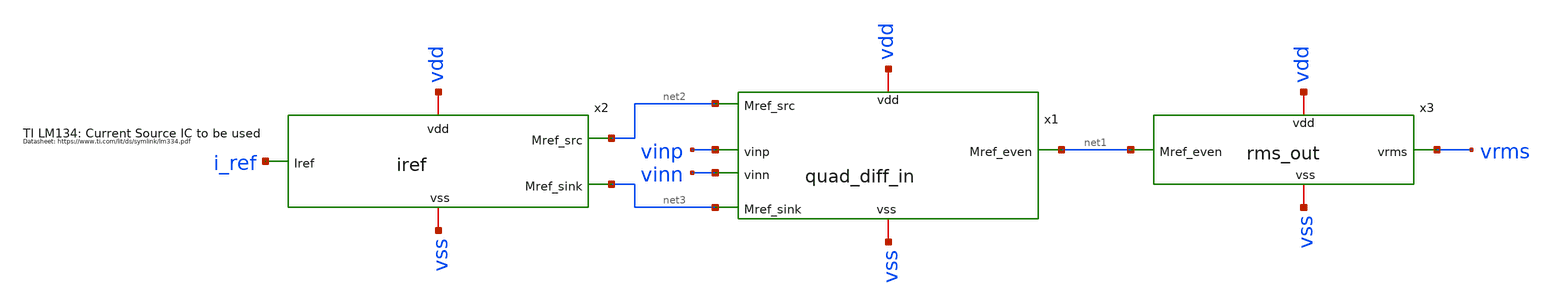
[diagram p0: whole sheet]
** sch_path: designs/libs/tb_analog/tb_rms_det/tb_rms_det.sch
**.subckt tb_rms_det
x1 vdd net2 net1 vinp vinn net3 vss quad_diff_in
x2 vdd net2 i_ref net3 vss iref
x3 vdd net1 vrms vss rms_out
**.ends

* expanding   symbol:  libs/core_analog/quad_diff_in/quad_diff_in.sym # of pins=7
** sym_path: designs/libs/core_analog/quad_diff_in/quad_diff_in.sym
** sch_path: designs/libs/core_analog/quad_diff_in/quad_diff_in.sch
.subckt quad_diff_in vdd Mref_src Mref_even vinp vinn Mref_sink vss
*.iopin vdd
*.iopin vss
*.ipin vinp
*.ipin vinn
*.ipin Mref_src
*.ipin Mref_sink
*.opin Mref_even
XM1 net3 vinp net2 vss nfet_03v3 L=0.28u W=0.22u nf=1 ad='int((nf+1)/2) * W/nf * 0.18u' as='int((nf+2)/2) * W/nf * 0.18u'
+ pd='2*int((nf+1)/2) * (W/nf + 0.18u)' ps='2*int((nf+2)/2) * (W/nf + 0.18u)' nrd='0.18u / W' nrs='0.18u / W'
+ sa=0 sb=0 sd=0 m=1
XM2 Mref_even Mref_even vdd vdd pfet_03v3 L=0.28u W=0.22u nf=1 ad='int((nf+1)/2) * W/nf * 0.18u' as='int((nf+2)/2) * W/nf * 0.18u'
+ pd='2*int((nf+1)/2) * (W/nf + 0.18u)' ps='2*int((nf+2)/2) * (W/nf + 0.18u)' nrd='0.18u / W' nrs='0.18u / W'
+ sa=0 sb=0 sd=0 m=1
XM3 net3 vinn net1 vss nfet_03v3 L=0.28u W=0.22u nf=1 ad='int((nf+1)/2) * W/nf * 0.18u' as='int((nf+2)/2) * W/nf * 0.18u'
+ pd='2*int((nf+1)/2) * (W/nf + 0.18u)' ps='2*int((nf+2)/2) * (W/nf + 0.18u)' nrd='0.18u / W' nrs='0.18u / W'
+ sa=0 sb=0 sd=0 m=1
XM4 vdd vinp net1 vss nfet_03v3 L=0.28u W=0.22u nf=1 ad='int((nf+1)/2) * W/nf * 0.18u' as='int((nf+2)/2) * W/nf * 0.18u'
+ pd='2*int((nf+1)/2) * (W/nf + 0.18u)' ps='2*int((nf+2)/2) * (W/nf + 0.18u)' nrd='0.18u / W' nrs='0.18u / W'
+ sa=0 sb=0 sd=0 m=1
XM5 vdd vinn net2 vss nfet_03v3 L=0.28u W=0.22u nf=1 ad='int((nf+1)/2) * W/nf * 0.18u' as='int((nf+2)/2) * W/nf * 0.18u'
+ pd='2*int((nf+1)/2) * (W/nf + 0.18u)' ps='2*int((nf+2)/2) * (W/nf + 0.18u)' nrd='0.18u / W' nrs='0.18u / W'
+ sa=0 sb=0 sd=0 m=1
even_curr Mref_even net3 0
.save i(even_curr)
XM6 net4 Mref_src vdd vdd pfet_03v3 L=0.28u W=0.22u nf=1 ad='int((nf+1)/2) * W/nf * 0.18u' as='int((nf+2)/2) * W/nf * 0.18u'
+ pd='2*int((nf+1)/2) * (W/nf + 0.18u)' ps='2*int((nf+2)/2) * (W/nf + 0.18u)' nrd='0.18u / W' nrs='0.18u / W'
+ sa=0 sb=0 sd=0 m=1
dc_bias net4 Mref_even 0
.save i(dc_bias)
XM7 net1 Mref_sink vss vss nfet_03v3 L=0.28u W=0.22u nf=1 ad='int((nf+1)/2) * W/nf * 0.18u' as='int((nf+2)/2) * W/nf * 0.18u'
+ pd='2*int((nf+1)/2) * (W/nf + 0.18u)' ps='2*int((nf+2)/2) * (W/nf + 0.18u)' nrd='0.18u / W' nrs='0.18u / W'
+ sa=0 sb=0 sd=0 m=1
XM8 net2 Mref_sink vss vss nfet_03v3 L=0.28u W=0.22u nf=1 ad='int((nf+1)/2) * W/nf * 0.18u' as='int((nf+2)/2) * W/nf * 0.18u'
+ pd='2*int((nf+1)/2) * (W/nf + 0.18u)' ps='2*int((nf+2)/2) * (W/nf + 0.18u)' nrd='0.18u / W' nrs='0.18u / W'
+ sa=0 sb=0 sd=0 m=1
.ends


* expanding   symbol:  libs/core_analog/iref/iref.sym # of pins=5
** sym_path: designs/libs/core_analog/iref/iref.sym
** sch_path: designs/libs/core_analog/iref/iref.sch
.subckt iref vdd Mref_src Iref Mref_sink vss
*.ipin Iref
*.iopin vdd
*.iopin vss
*.opin Mref_src
*.opin Mref_sink
XM1 Iref Iref vss vss nfet_03v3 L=0.28u W=0.22u nf=1 ad='int((nf+1)/2) * W/nf * 0.18u' as='int((nf+2)/2) * W/nf * 0.18u'
+ pd='2*int((nf+1)/2) * (W/nf + 0.18u)' ps='2*int((nf+2)/2) * (W/nf + 0.18u)' nrd='0.18u / W' nrs='0.18u / W'
+ sa=0 sb=0 sd=0 m=1
XM2 Mref_src Mref_src vdd net1 pfet_03v3 L=0.28u W=0.22u nf=1 ad='int((nf+1)/2) * W/nf * 0.18u' as='int((nf+2)/2) * W/nf * 0.18u'
+ pd='2*int((nf+1)/2) * (W/nf + 0.18u)' ps='2*int((nf+2)/2) * (W/nf + 0.18u)' nrd='0.18u / W' nrs='0.18u / W'
+ sa=0 sb=0 sd=0 m=1
XM3 Mref_src Iref vss vss nfet_03v3 L=0.28u W=0.22u nf=1 ad='int((nf+1)/2) * W/nf * 0.18u' as='int((nf+2)/2) * W/nf * 0.18u'
+ pd='2*int((nf+1)/2) * (W/nf + 0.18u)' ps='2*int((nf+2)/2) * (W/nf + 0.18u)' nrd='0.18u / W' nrs='0.18u / W'
+ sa=0 sb=0 sd=0 m=1
.ends


* expanding   symbol:  libs/core_analog/rms_out/rms_out.sym # of pins=4
** sym_path: designs/libs/core_analog/rms_out/rms_out.sym
** sch_path: designs/libs/core_analog/rms_out/rms_out.sch
.subckt rms_out vdd Mref_even vrms vss
*.ipin Mref_even
*.iopin vdd
*.iopin vss
*.opin vrms
XM1 net1 Mref_even vdd vdd pfet_03v3 L=0.28u W=0.22u nf=1 ad='int((nf+1)/2) * W/nf * 0.18u' as='int((nf+2)/2) * W/nf * 0.18u'
+ pd='2*int((nf+1)/2) * (W/nf + 0.18u)' ps='2*int((nf+2)/2) * (W/nf + 0.18u)' nrd='0.18u / W' nrs='0.18u / W'
+ sa=0 sb=0 sd=0 m=1
ieven_mirror net1 vrms 0
.save i(ieven_mirror)
XM2 vrms vrms vss vss nfet_03v3 L=0.28u W=0.22u nf=1 ad='int((nf+1)/2) * W/nf * 0.18u' as='int((nf+2)/2) * W/nf * 0.18u'
+ pd='2*int((nf+1)/2) * (W/nf + 0.18u)' ps='2*int((nf+2)/2) * (W/nf + 0.18u)' nrd='0.18u / W' nrs='0.18u / W'
+ sa=0 sb=0 sd=0 m=1
.ends

.end
